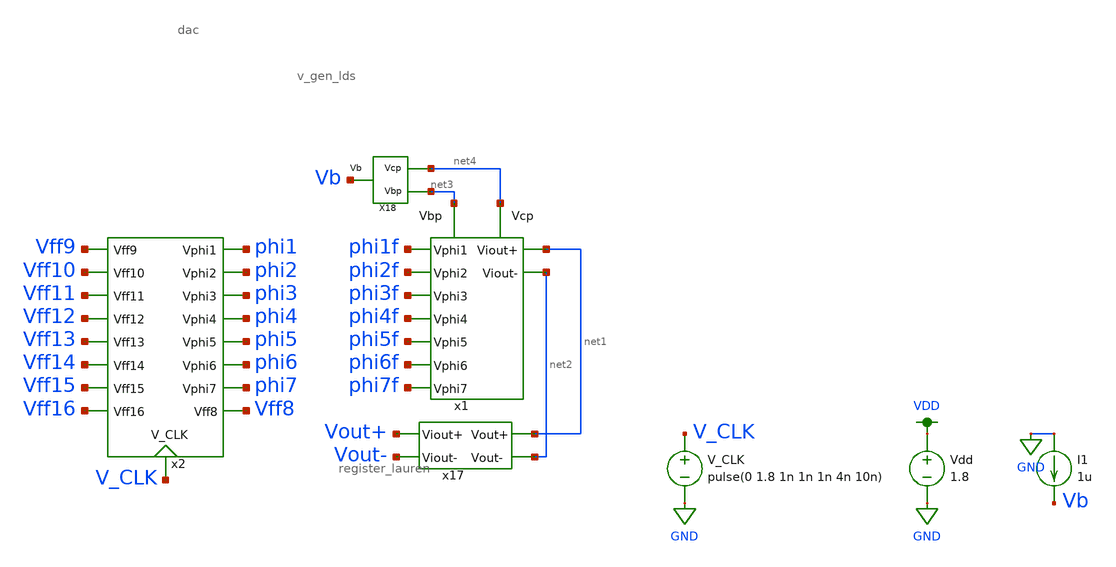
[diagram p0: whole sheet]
** sch_path: simulation/post_layout_sim/register_dac_mc_lauren.sch
**.subckt register_dac_mc_lauren
V_CLK V_CLK GND pulse(0 1.8 1n 1n 1n 4n 10n)
Vdd VDD GND 1.8
x1 phi1f phi2f phi3f phi4f phi5f phi6f phi7f net1 net2 net3 net4 dac
x2 Vff10 Vff11 Vff12 Vff13 Vff14 Vff16 Vff15 Vff9 phi1 phi2 phi3 phi4 phi5 phi6 phi7 Vff8 V_CLK
+ register_lauren
X18 net4 net3 Vb v_gen_lds
I1 GND Vb 1u
x17 Vout+ Vout- net1 net2 filter_lvs
**** begin user architecture code

.option wnflag=1
.param MC_SWITCH=0.0
.lib ~/skywater/skywater-pdk/libraries/sky130_fd_pr_ngspice/latest/models/sky130.lib.spice tt



.ic v(phi1)=0 v(phi2)=0 v(phi3)=0 v(phi4)=0 v(phi5)=0 v(phi6)=0 v(phi7)=0 v(Vff8)=0 v(Vff9)=1.8
+ v(Vff10)=1.8 v(Vff11)=1.8 v(Vff12)=1.8 v(Vff13)=1.8 v(Vff14)=1.8 v(Vff15)=1.8 v(Vff16)=1.8
.control
  set wr_vecnames
  set wr_singlescale

  let mc_runs = 10
  let run = 1
  dowhile run <= mc_runs
    tran 0.1n 1u
    wrdata ~/VLSI_Sine_Gen/simulation/sim_data/mc_data/register_dac_mc_m0{$&run}.txt v(Vout+) v(Vout-)
+ v(Vout+)-v(Vout-)
    reset
    let run = run + 1
  end
  quit
.endc


**** end user architecture code
**.ends
.GLOBAL GND
.GLOBAL VDD
.end
